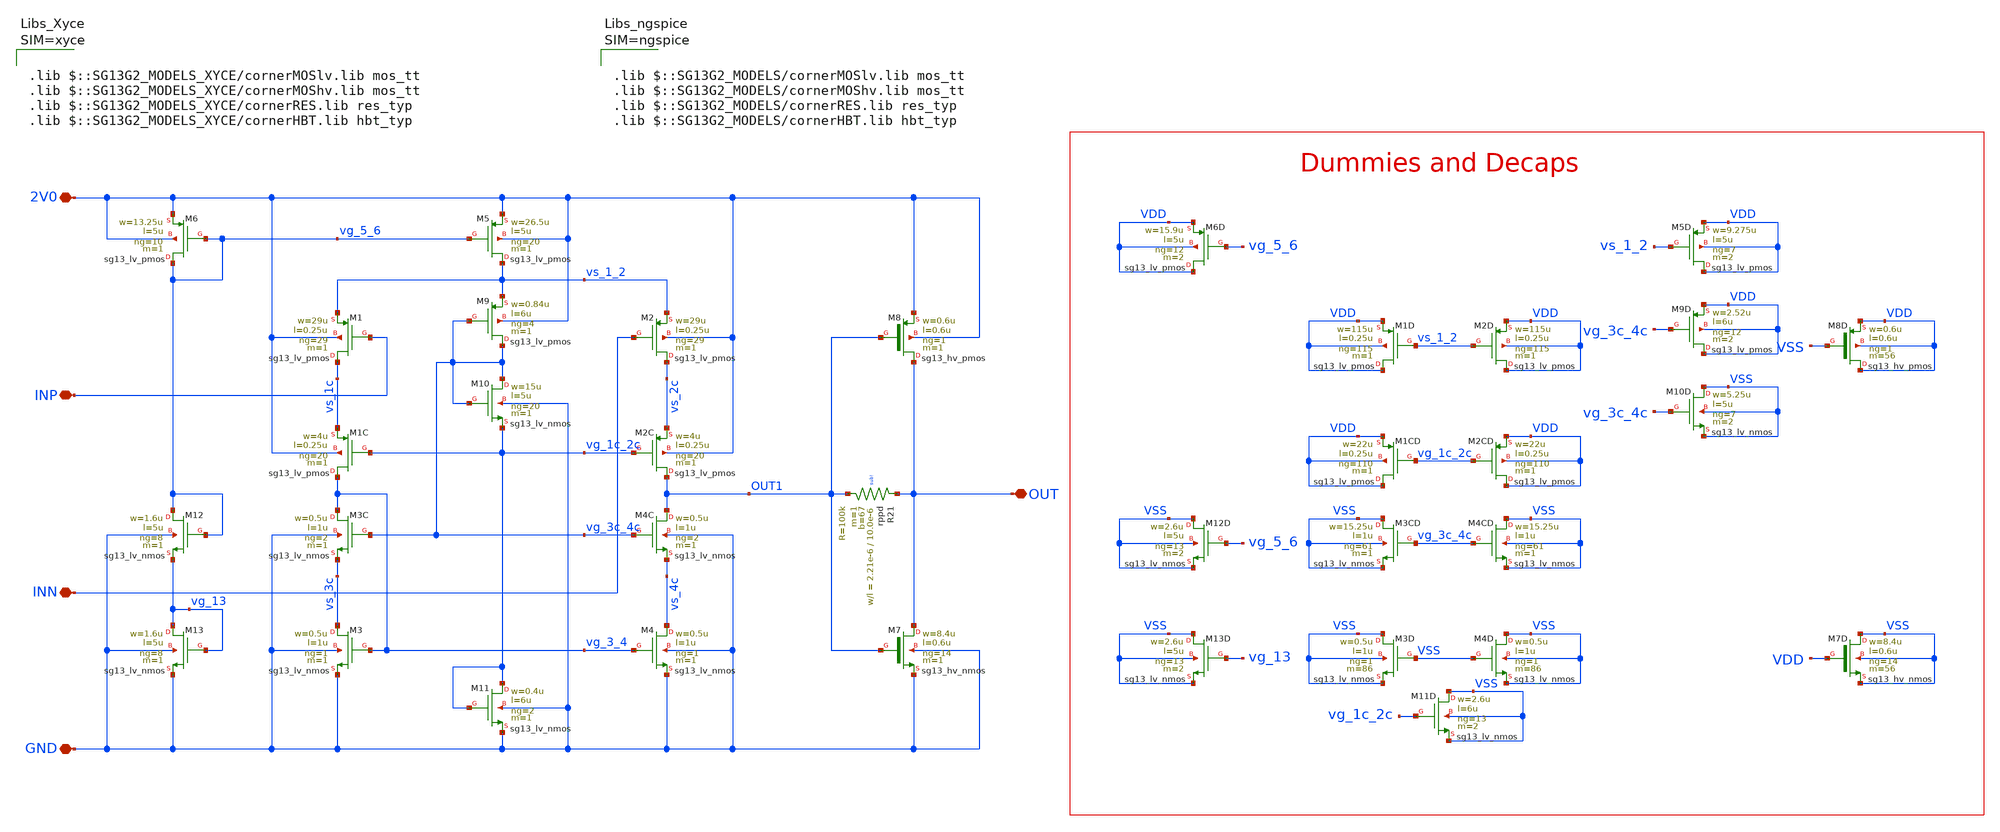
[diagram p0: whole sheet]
** sch_path: mWATTBAT/design_data/xschem/IFAMP.sch
**.subckt IFAMP INP INN OUT 2V0 GND
*.iopin INP
*.iopin INN
*.iopin OUT
*.iopin 2V0
*.iopin GND
XM1 vs_1c INP vs_1_2 2V0 sg13_lv_pmos w=29u l=0.25u ng=29 m=1 mm_ok=1
XM2 vs_2c INN vs_1_2 2V0 sg13_lv_pmos w=29u l=0.25u ng=29 m=1 mm_ok=1
XM1C vg_3_4 vg_1c_2c vs_1c 2V0 sg13_lv_pmos w=4u l=0.25u ng=20 m=1 mm_ok=1
XM2C OUT1 vg_1c_2c vs_2c 2V0 sg13_lv_pmos w=4u l=0.25u ng=20 m=1 mm_ok=1
XM3C vg_3_4 vg_3c_4c vs_3c GND sg13_lv_nmos w=0.5u l=1u ng=2 m=1 mm_ok=1
XM4C OUT1 vg_3c_4c vs_4c GND sg13_lv_nmos w=0.5u l=1u ng=2 m=1 mm_ok=1
XM3 vs_3c vg_3_4 GND GND sg13_lv_nmos w=0.5u l=1u ng=1 m=1 mm_ok=1
XM4 vs_4c vg_3_4 GND GND sg13_lv_nmos w=0.5u l=1u ng=1 m=1 mm_ok=1
XM5 vs_1_2 vg_5_6 2V0 2V0 sg13_lv_pmos w=26.5u l=5u ng=20 m=1 mm_ok=1
XM6 vg_5_6 vg_5_6 2V0 2V0 sg13_lv_pmos w=13.25u l=5u ng=10 m=1 mm_ok=1
XM7 OUT OUT1 GND GND sg13_hv_nmos w=8.4u l=0.6u ng=14 m=1 mm_ok=1
XM8 OUT OUT1 2V0 2V0 sg13_hv_pmos w=0.6u l=0.6u ng=1 m=1 mm_ok=1
XM9 vg_3c_4c vg_3c_4c vs_1_2 2V0 sg13_lv_pmos w=0.84u l=6u ng=4 m=1 mm_ok=1
XM10 vg_3c_4c vg_3c_4c vg_1c_2c GND sg13_lv_nmos w=15u l=5u ng=20 m=1 mm_ok=1
XM11 vg_1c_2c vg_1c_2c GND GND sg13_lv_nmos w=0.4u l=6u ng=2 m=1 mm_ok=1
XM13 vg_13 vg_13 GND GND sg13_lv_nmos w=1.6u l=5u ng=8 m=1 mm_ok=1
XM12 vg_5_6 vg_5_6 vg_13 GND sg13_lv_nmos w=1.6u l=5u ng=8 m=1 mm_ok=1
XM13D VSS vg_13 VSS VSS sg13_lv_nmos w=2.6u l=5u ng=13 m=2 mm_ok=1
XM12D VSS vg_5_6 VSS VSS sg13_lv_nmos w=2.6u l=5u ng=13 m=2 mm_ok=1
XM6D VDD vg_5_6 VDD VDD sg13_lv_pmos w=15.9u l=5u ng=12 m=2 mm_ok=1
XM5D VDD vs_1_2 VDD VDD sg13_lv_pmos w=9.275u l=5u ng=7 m=2 mm_ok=1
XM11D VSS vg_1c_2c VSS VSS sg13_lv_nmos w=2.6u l=6u ng=13 m=2 mm_ok=1
XM9D VDD vg_3c_4c VDD VDD sg13_lv_pmos w=2.52u l=6u ng=12 m=2 mm_ok=1
XM10D VSS vg_3c_4c VSS VSS sg13_lv_nmos w=5.25u l=5u ng=7 m=2 mm_ok=1
XM3CD VSS vg_3c_4c VSS VSS sg13_lv_nmos w=15.25u l=1u ng=61 m=1 mm_ok=1
XM3D VSS VSS VSS VSS sg13_lv_nmos w=0.5u l=1u ng=1 m=86 mm_ok=1
XM4CD VSS vg_3c_4c VSS VSS sg13_lv_nmos w=15.25u l=1u ng=61 m=1 mm_ok=1
XM1CD VDD vg_1c_2c VDD VDD sg13_lv_pmos w=22u l=0.25u ng=110 m=1 mm_ok=1
XM2CD VDD vg_1c_2c VDD VDD sg13_lv_pmos w=22u l=0.25u ng=110 m=1 mm_ok=1
XM1D VDD vs_1_2 VDD VDD sg13_lv_pmos w=115u l=0.25u ng=115 m=1 mm_ok=1
XM2D VDD vs_1_2 VDD VDD sg13_lv_pmos w=115u l=0.25u ng=115 m=1 mm_ok=1
XM4D VSS VSS VSS VSS sg13_lv_nmos w=0.5u l=1u ng=1 m=86 mm_ok=1
XM7D VSS VDD VSS VSS sg13_hv_nmos w=8.4u l=0.6u ng=14 m=56 mm_ok=1
XM8D VDD VSS VDD VDD sg13_hv_pmos w=0.6u l=0.6u ng=1 m=56 mm_ok=1
XR21 OUT OUT1 sub! rppd w=2.21e-6 l=10.0e-6 m=1 b=67 mm_ok=1
**** begin user architecture code






.lib $::SG13G2_MODELS/cornerMOSlv.lib mos_tt
.lib $::SG13G2_MODELS/cornerMOShv.lib mos_tt
.lib $::SG13G2_MODELS/cornerRES.lib res_typ
.lib $::SG13G2_MODELS/cornerHBT.lib hbt_typ



**** end user architecture code
**.ends
.end
